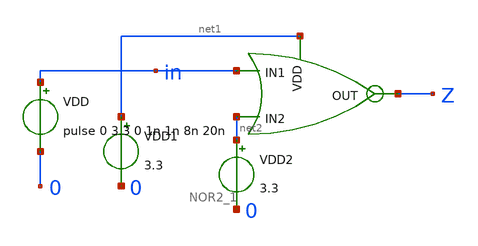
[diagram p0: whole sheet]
** sch_path: chipathon_2023/initial_notebooks_2023/accepted_notebooks/Current-Steering-DAC/DAC/Test_NOR2_1.sch
**.subckt Test_NOR2_1
VDD in 0 pulse 0 3.3 0 1n 1n 8n 20n
VDD1 net1 0 3.3
VDD2 net2 0 3.3
x1 net1 in Z net2 NOR2_1
**** begin user architecture code




.include /foss/pdks/gf180mcuC/libs.tech/ngspice/design.ngspice
.lib /foss/pdks/gf180mcuC/libs.tech/ngspice/sm141064.ngspice typical

.control
	*dc vin 0 3.3 0.01
	tran 0.1n 40n
	plot V(in) V(z)
.endc
.save all




**** end user architecture code
**.ends
.end
